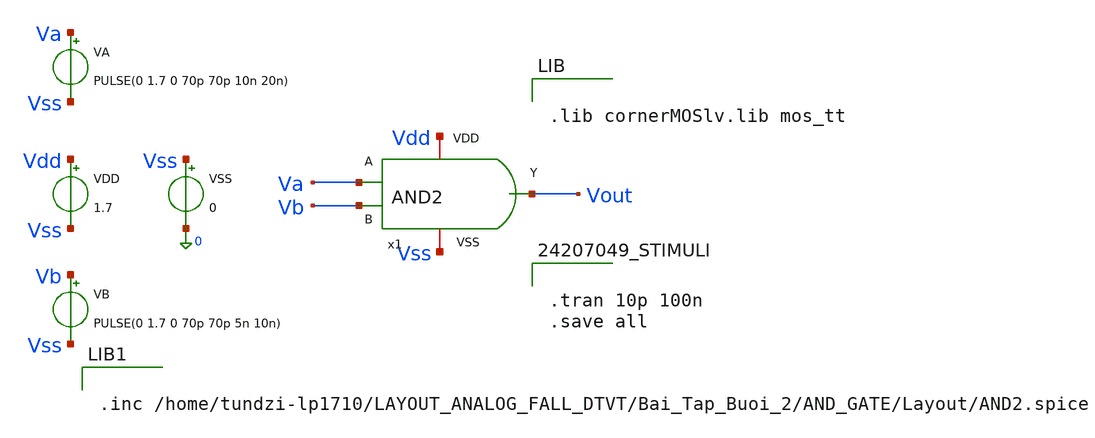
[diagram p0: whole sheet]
** sch_path: logic_gate/AND2/LAYOUT_POST-SIMULATION/AND2_tb.sch
**.subckt AND2_tb
VDD Vdd Vss 1.7
VSS Vss 0 0
VA Va Vss PULSE(0 1.7 0 70p 70p 10n 20n)
VB Vb Vss PULSE(0 1.7 0 70p 70p 5n 10n)
x1 Va Vb Vout Vdd Vss AND2
**** begin user architecture code


.lib cornerMOSlv.lib mos_tt




.tran 10p 100n
.save all




.inc /home/tundzi-lp1710/LAYOUT_ANALOG_FALL_DTVT/Bai_Tap_Buoi_2/AND_GATE/Layout/AND2.spice


**** end user architecture code
**.ends
.end
